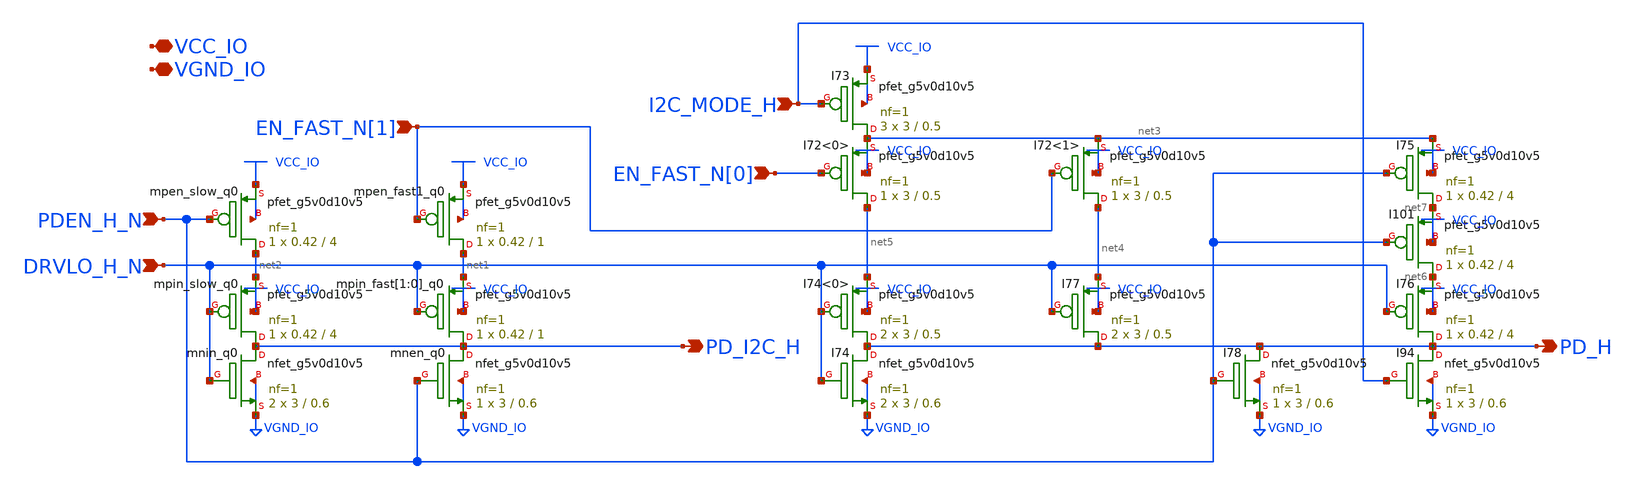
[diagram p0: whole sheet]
** sch_path: gpiov2_pdpredrvr_strong_nr2.sch
* Copyright 2023 David Mitchell Bailey
* Licensed under the Apache License, Version 2.0 (the "License");
* you may not use this file except in compliance with the License.
* You may obtain a copy of the License at
* https://www.apache.org/licenses/LICENSE-2.0
* Unless required by applicable law or agreed to in writing, software
* distributed under the License is distributed on an "AS IS" BASIS,
* WITHOUT WARRANTIES OR CONDITIONS OF ANY KIND, either express or implied.
* See the License for the specific language governing permissions and
* limitations under the License.
**.subckt gpiov2_pdpredrvr_strong_nr2 PDEN_H_N VCC_IO VGND_IO PD_I2C_H DRVLO_H_N I2C_MODE_H
*+ EN_FAST_N[1] EN_FAST_N[0] PD_H
*.ipin PDEN_H_N
*.iopin VCC_IO
*.iopin VGND_IO
*.opin PD_I2C_H
*.ipin DRVLO_H_N
*.ipin I2C_MODE_H
*.ipin EN_FAST_N[1]
*.ipin EN_FAST_N[0]
*.opin PD_H
Xmpin_slow_q0 PD_I2C_H DRVLO_H_N net2 VCC_IO sky130_fd_pr__pfet_g5v0d10v5 L=4 W=0.42 nf=1 ad='int((nf+1)/2) * W/nf * 0.29'
+ as='int((nf+2)/2) * W/nf * 0.29' pd='2*int((nf+1)/2) * (W/nf + 0.29)' ps='2*int((nf+2)/2) * (W/nf + 0.29)'
+ nrd='0.29 / W' nrs='0.29 / W' sa=0 sb=0 sd=0 mult=1 m=1
Xmpen_slow_q0 net2 PDEN_H_N VCC_IO VCC_IO sky130_fd_pr__pfet_g5v0d10v5 L=4 W=0.42 nf=1 ad='int((nf+1)/2) * W/nf * 0.29'
+ as='int((nf+2)/2) * W/nf * 0.29' pd='2*int((nf+1)/2) * (W/nf + 0.29)' ps='2*int((nf+2)/2) * (W/nf + 0.29)'
+ nrd='0.29 / W' nrs='0.29 / W' sa=0 sb=0 sd=0 mult=1 m=1
Xmpin_fast[1]_q0 PD_I2C_H DRVLO_H_N net1 VCC_IO sky130_fd_pr__pfet_g5v0d10v5 L=1 W=0.42 nf=1 ad='int((nf+1)/2) * W/nf * 0.29'
+ as='int((nf+2)/2) * W/nf * 0.29' pd='2*int((nf+1)/2) * (W/nf + 0.29)' ps='2*int((nf+2)/2) * (W/nf + 0.29)'
+ nrd='0.29 / W' nrs='0.29 / W' sa=0 sb=0 sd=0 mult=1 m=1
Xmpin_fast[0]_q0 PD_I2C_H DRVLO_H_N net1 VCC_IO sky130_fd_pr__pfet_g5v0d10v5 L=1 W=0.42 nf=1 ad='int((nf+1)/2) * W/nf * 0.29'
+ as='int((nf+2)/2) * W/nf * 0.29' pd='2*int((nf+1)/2) * (W/nf + 0.29)' ps='2*int((nf+2)/2) * (W/nf + 0.29)'
+ nrd='0.29 / W' nrs='0.29 / W' sa=0 sb=0 sd=0 mult=1 m=1
Xmpen_fast1_q0 net1 EN_FAST_N[1] VCC_IO VCC_IO sky130_fd_pr__pfet_g5v0d10v5 L=1 W=0.42 nf=1 ad='int((nf+1)/2) * W/nf * 0.29'
+ as='int((nf+2)/2) * W/nf * 0.29' pd='2*int((nf+1)/2) * (W/nf + 0.29)' ps='2*int((nf+2)/2) * (W/nf + 0.29)'
+ nrd='0.29 / W' nrs='0.29 / W' sa=0 sb=0 sd=0 mult=1 m=1
Xmnin_q0 PD_I2C_H DRVLO_H_N VGND_IO VGND_IO sky130_fd_pr__nfet_g5v0d10v5 L=0.6 W=3 nf=1 ad='int((nf+1)/2) * W/nf * 0.29'
+ as='int((nf+2)/2) * W/nf * 0.29' pd='2*int((nf+1)/2) * (W/nf + 0.29)' ps='2*int((nf+2)/2) * (W/nf + 0.29)'
+ nrd='0.29 / W' nrs='0.29 / W' sa=0 sb=0 sd=0 mult=2 m=2
Xmnen_q0 PD_I2C_H PDEN_H_N VGND_IO VGND_IO sky130_fd_pr__nfet_g5v0d10v5 L=0.6 W=3 nf=1 ad='int((nf+1)/2) * W/nf * 0.29'
+ as='int((nf+2)/2) * W/nf * 0.29' pd='2*int((nf+1)/2) * (W/nf + 0.29)' ps='2*int((nf+2)/2) * (W/nf + 0.29)'
+ nrd='0.29 / W' nrs='0.29 / W' sa=0 sb=0 sd=0 mult=1 m=1
XI74<0> PD_H DRVLO_H_N net5 VCC_IO sky130_fd_pr__pfet_g5v0d10v5 L=0.5 W=3 nf=1 ad='int((nf+1)/2) * W/nf * 0.29'
+ as='int((nf+2)/2) * W/nf * 0.29' pd='2*int((nf+1)/2) * (W/nf + 0.29)' ps='2*int((nf+2)/2) * (W/nf + 0.29)'
+ nrd='0.29 / W' nrs='0.29 / W' sa=0 sb=0 sd=0 mult=2 m=2
XI73 net3 I2C_MODE_H VCC_IO VCC_IO sky130_fd_pr__pfet_g5v0d10v5 L=0.5 W=3 nf=1 ad='int((nf+1)/2) * W/nf * 0.29'
+ as='int((nf+2)/2) * W/nf * 0.29' pd='2*int((nf+1)/2) * (W/nf + 0.29)' ps='2*int((nf+2)/2) * (W/nf + 0.29)'
+ nrd='0.29 / W' nrs='0.29 / W' sa=0 sb=0 sd=0 mult=3 m=3
XI76 PD_H DRVLO_H_N net6 VCC_IO sky130_fd_pr__pfet_g5v0d10v5 L=4 W=0.42 nf=1 ad='int((nf+1)/2) * W/nf * 0.29'
+ as='int((nf+2)/2) * W/nf * 0.29' pd='2*int((nf+1)/2) * (W/nf + 0.29)' ps='2*int((nf+2)/2) * (W/nf + 0.29)'
+ nrd='0.29 / W' nrs='0.29 / W' sa=0 sb=0 sd=0 mult=1 m=1
XI101 net6 PDEN_H_N net7 VCC_IO sky130_fd_pr__pfet_g5v0d10v5 L=4 W=0.42 nf=1 ad='int((nf+1)/2) * W/nf * 0.29'
+ as='int((nf+2)/2) * W/nf * 0.29' pd='2*int((nf+1)/2) * (W/nf + 0.29)' ps='2*int((nf+2)/2) * (W/nf + 0.29)'
+ nrd='0.29 / W' nrs='0.29 / W' sa=0 sb=0 sd=0 mult=1 m=1
XI74 PD_H DRVLO_H_N VGND_IO VGND_IO sky130_fd_pr__nfet_g5v0d10v5 L=0.6 W=3 nf=1 ad='int((nf+1)/2) * W/nf * 0.29'
+ as='int((nf+2)/2) * W/nf * 0.29' pd='2*int((nf+1)/2) * (W/nf + 0.29)' ps='2*int((nf+2)/2) * (W/nf + 0.29)'
+ nrd='0.29 / W' nrs='0.29 / W' sa=0 sb=0 sd=0 mult=2 m=2
XI94 PD_H I2C_MODE_H VGND_IO VGND_IO sky130_fd_pr__nfet_g5v0d10v5 L=0.6 W=3 nf=1 ad='int((nf+1)/2) * W/nf * 0.29'
+ as='int((nf+2)/2) * W/nf * 0.29' pd='2*int((nf+1)/2) * (W/nf + 0.29)' ps='2*int((nf+2)/2) * (W/nf + 0.29)'
+ nrd='0.29 / W' nrs='0.29 / W' sa=0 sb=0 sd=0 mult=1 m=1
XI72<0> net5 EN_FAST_N[0] net3 VCC_IO sky130_fd_pr__pfet_g5v0d10v5 L=0.5 W=3 nf=1 ad='int((nf+1)/2) * W/nf * 0.29'
+ as='int((nf+2)/2) * W/nf * 0.29' pd='2*int((nf+1)/2) * (W/nf + 0.29)' ps='2*int((nf+2)/2) * (W/nf + 0.29)'
+ nrd='0.29 / W' nrs='0.29 / W' sa=0 sb=0 sd=0 mult=1 m=1
XI75 net7 PDEN_H_N net3 VCC_IO sky130_fd_pr__pfet_g5v0d10v5 L=4 W=0.42 nf=1 ad='int((nf+1)/2) * W/nf * 0.29'
+ as='int((nf+2)/2) * W/nf * 0.29' pd='2*int((nf+1)/2) * (W/nf + 0.29)' ps='2*int((nf+2)/2) * (W/nf + 0.29)'
+ nrd='0.29 / W' nrs='0.29 / W' sa=0 sb=0 sd=0 mult=1 m=1
XI78 PD_H PDEN_H_N VGND_IO VGND_IO sky130_fd_pr__nfet_g5v0d10v5 L=0.6 W=3 nf=1 ad='int((nf+1)/2) * W/nf * 0.29'
+ as='int((nf+2)/2) * W/nf * 0.29' pd='2*int((nf+1)/2) * (W/nf + 0.29)' ps='2*int((nf+2)/2) * (W/nf + 0.29)'
+ nrd='0.29 / W' nrs='0.29 / W' sa=0 sb=0 sd=0 mult=1 m=1
XI77 PD_H DRVLO_H_N net4 VCC_IO sky130_fd_pr__pfet_g5v0d10v5 L=0.5 W=3 nf=1 ad='int((nf+1)/2) * W/nf * 0.29'
+ as='int((nf+2)/2) * W/nf * 0.29' pd='2*int((nf+1)/2) * (W/nf + 0.29)' ps='2*int((nf+2)/2) * (W/nf + 0.29)'
+ nrd='0.29 / W' nrs='0.29 / W' sa=0 sb=0 sd=0 mult=2 m=2
XI72<1> net4 EN_FAST_N[1] net3 VCC_IO sky130_fd_pr__pfet_g5v0d10v5 L=0.5 W=3 nf=1 ad='int((nf+1)/2) * W/nf * 0.29'
+ as='int((nf+2)/2) * W/nf * 0.29' pd='2*int((nf+1)/2) * (W/nf + 0.29)' ps='2*int((nf+2)/2) * (W/nf + 0.29)'
+ nrd='0.29 / W' nrs='0.29 / W' sa=0 sb=0 sd=0 mult=1 m=1
**.ends
.end
